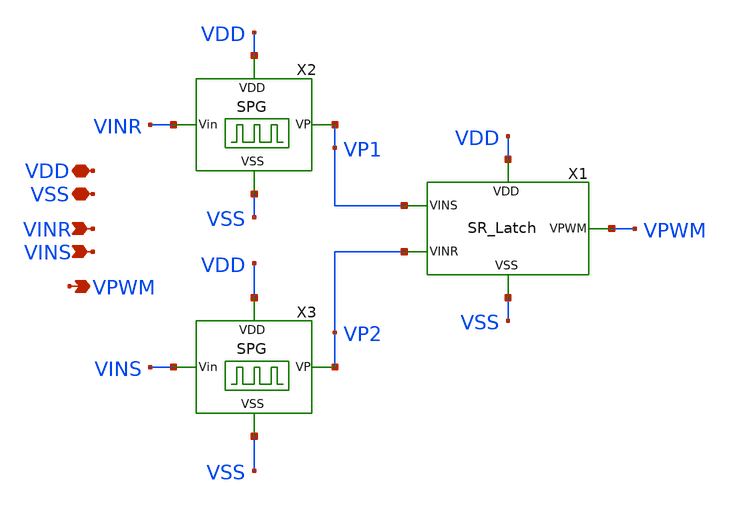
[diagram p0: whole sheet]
** sch_path: xschem/PD/PD.sch
**.subckt PD VDD VINR VPWM VSS VINS
*.iopin VDD
*.ipin VINR
*.opin VPWM
*.iopin VSS
*.ipin VINS
X1 VPWM VP1 VDD VSS VP2 SR_Latch
X2 VP1 VINR VDD VSS SPG
X3 VP2 VINS VDD VSS SPG
**** begin user architecture code



**** end user architecture code
**.ends

* expanding   symbol:  ../SR_Latch_NOR/SR_Latch.sym # of pins=5
** sym_path: xschem/SR_Latch_NOR/SR_Latch.sym
** sch_path: xschem/SR_Latch_NOR/SR_Latch.sch
.subckt SR_Latch VPWM VINS VDD VSS VINR
*.iopin VDD
*.ipin VINS
*.iopin VSS
*.opin VPWM
*.ipin VINR
X1 VDD VSS V_N VINS VPWM NOR
X2 VDD VSS VPWM V_N VINR NOR
**** begin user architecture code



**** end user architecture code
.ends


* expanding   symbol:  ../SPG/SPG.sym # of pins=4
** sym_path: xschem/SPG/SPG.sym
** sch_path: xschem/SPG/SPG.sch
.subckt SPG VP Vin VDD VSS
*.iopin VDD
*.ipin Vin
*.opin VP
*.iopin VSS
R1 B1 net1 {R_del} m=1
C4 B1 VSS {C_del} m=1
X1 Vin net3 VDD VSS INV
X2 A B VSS VDD VP AND
X3 net3 B VDD VSS INV
X4 B net1 VDD VSS INV
X5 B1 net2 VDD VSS INV
X6 net2 A VDD VSS INV
**** begin user architecture code



**** end user architecture code
.ends


* expanding   symbol:  ../DigitalGates/NOR.sym # of pins=5
** sym_path: xschem/DigitalGates/NOR.sym
** sch_path: xschem/DigitalGates/NOR.sch
.subckt NOR VDD VSS F X Y
*.iopin VDD
*.ipin X
*.opin F
*.iopin VSS
*.ipin Y
XM4 F Y net1 VDD sg13_lv_pmos w=0.15u l=0.13u ng=1 m=6 mm_ok=1
XM3 F X VSS VSS sg13_lv_nmos w=0.15u l=0.13u ng=1 m=1 mm_ok=1
XM1 F Y VSS VSS sg13_lv_nmos w=0.15u l=0.13u ng=1 m=1 mm_ok=1
XM2 net1 X VDD VDD sg13_lv_pmos w=0.15u l=0.13u ng=1 m=6 mm_ok=1
**** begin user architecture code



**** end user architecture code
.ends


* expanding   symbol:  ../DigitalGates/INV.sym # of pins=4
** sym_path: xschem/DigitalGates/INV.sym
** sch_path: xschem/DigitalGates/INV.sch
.subckt INV X Y VDD VSS
*.iopin VDD
*.ipin X
*.opin Y
*.iopin VSS
XM3 Y X VSS VSS sg13_lv_nmos w={w_inv} l={l_inv} ng=1 m={mult} mm_ok=1
XM4 Y X VDD VDD sg13_lv_pmos w={w_inv} l={l_inv} ng=1 m={mult*3} mm_ok=1
**** begin user architecture code



**** end user architecture code
.ends


* expanding   symbol:  ../DigitalGates/AND.sym # of pins=5
** sym_path: xschem/DigitalGates/AND.sym
** sch_path: xschem/DigitalGates/AND.sch
.subckt AND X Y VSS VDD F
*.iopin VDD
*.ipin X
*.opin F
*.iopin VSS
*.ipin Y
XM1 net1 X net2 VSS sg13_lv_nmos w={w_N_AND} l={l_N_AND} ng=1 m={mult} mm_ok=1
XM2 F net1 VDD VDD sg13_lv_pmos w={w_P_AND} l={l_P_AND} ng=1 m={mult*3} mm_ok=1
XM3 net2 Y VSS VSS sg13_lv_nmos w={w_N_AND} l={l_N_AND} ng=1 m={mult} mm_ok=1
XM4 F net1 VSS VSS sg13_lv_nmos w={w_N_AND} l={l_N_AND} ng=1 m={mult} mm_ok=1
XM5 net1 Y VDD VDD sg13_lv_pmos w={w_P_AND} l={l_P_AND} ng=1 m={mult*3} mm_ok=1
XM6 net1 X VDD VDD sg13_lv_pmos w={w_P_AND} l={l_P_AND} ng=1 m={mult*3} mm_ok=1
**** begin user architecture code



**** end user architecture code
.ends

.end
